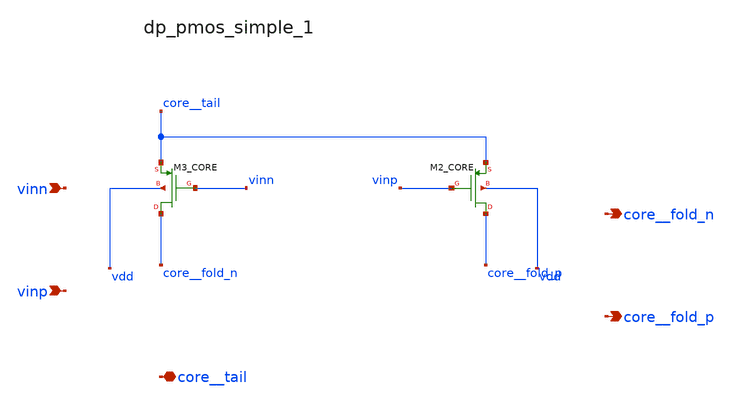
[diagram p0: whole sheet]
** sch_path: analog-db/raw/amp_035_fan_chopper_cmfb_dual/hier/blocks/dp_pmos_simple_1.sch
**.subckt dp_pmos_simple_1 vinn vinp core__tail core__fold_n core__fold_p
*.ipin vinn
*.ipin vinp
*.iopin core__tail
*.opin core__fold_n
*.opin core__fold_p
XM2_CORE core__fold_p vinp core__tail vdd sg13_lv_pmos w=x_dut_xm2_core_w l=x_dut_xm2_core_l ng=1
+ m=x_dut_xm2_core_m
XM3_CORE core__fold_n vinn core__tail vdd sg13_lv_pmos w=x_dut_xm3_core_w l=x_dut_xm3_core_l ng=1
+ m=x_dut_xm3_core_m
**.ends
.end
